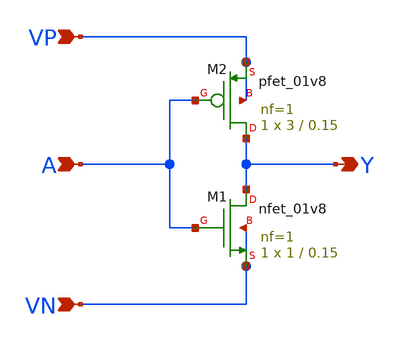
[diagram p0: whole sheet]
** sch_path: APIC-UTS/schematic/goldwin_not/goldwin_not.sch
**.subckt goldwin_not A VP VN Y
*.ipin A
*.ipin VP
*.ipin VN
*.opin Y
XM1 Y A VN VN sky130_fd_pr__nfet_01v8 L=0.15 W=1 nf=1 ad='int((nf+1)/2) * W/nf * 0.29' as='int((nf+2)/2) * W/nf * 0.29'
+ pd='2*int((nf+1)/2) * (W/nf + 0.29)' ps='2*int((nf+2)/2) * (W/nf + 0.29)' nrd='0.29 / W' nrs='0.29 / W'
+ sa=0 sb=0 sd=0 mult=1 m=1
XM2 Y A VP VP sky130_fd_pr__pfet_01v8 L=0.15 W=3 nf=1 ad='int((nf+1)/2) * W/nf * 0.29' as='int((nf+2)/2) * W/nf * 0.29'
+ pd='2*int((nf+1)/2) * (W/nf + 0.29)' ps='2*int((nf+2)/2) * (W/nf + 0.29)' nrd='0.29 / W' nrs='0.29 / W'
+ sa=0 sb=0 sd=0 mult=1 m=1
**.ends
.end
